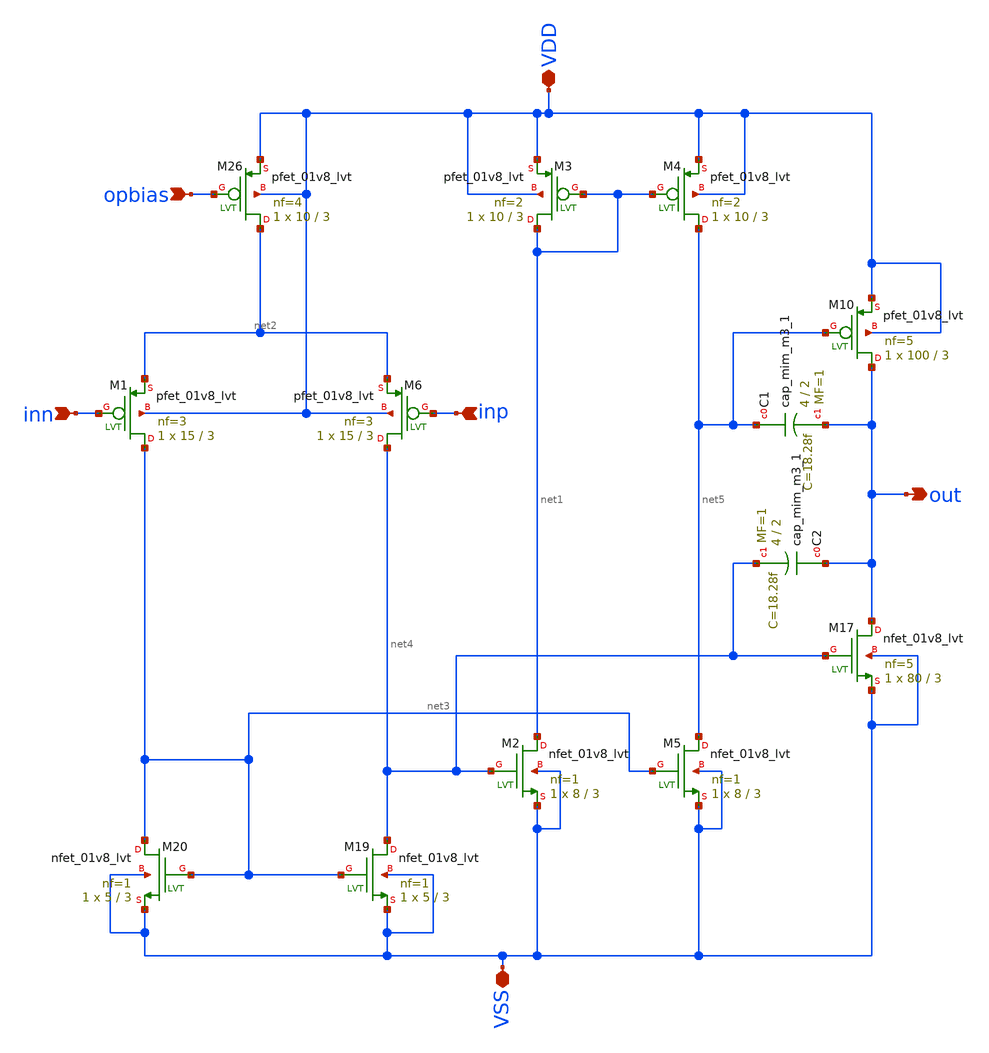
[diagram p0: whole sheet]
** sch_path: xschem/opamp/opamp.sch
**.subckt opamp inp inn opbias out VDD VSS
*.ipin inp
*.ipin inn
*.ipin opbias
*.opin out
*.iopin VDD
*.iopin VSS
XC1 net5 out sky130_fd_pr__cap_mim_m3_1 W=4 L=2 MF=1 m=1
XC2 out net4 sky130_fd_pr__cap_mim_m3_1 W=4 L=2 MF=1 m=1
XM26 net2 opbias VDD VDD sky130_fd_pr__pfet_01v8_lvt L=3 W=10 nf=4 ad='int((4 + 1)/2) * 10 / 4 * 0.29'
+ as='int((4 + 2)/2) * 10 / 4 * 0.29' pd='2*int((4 + 1)/2) * (10 / 4 + 0.29)' ps='2*int((4 + 2)/2) * (10 / 4 + 0.29)'
+ nrd='0.29 / 10 ' nrs='0.29 / 10 ' sa=0 sb=0 sd=0 mult=1 m=1
XM3 net1 net1 VDD VDD sky130_fd_pr__pfet_01v8_lvt L=3 W=10 nf=2 ad='int((2 + 1)/2) * 10 / 2 * 0.29' as='int((2 + 2)/2) * 10 / 2 * 0.29'
+ pd='2*int((2 + 1)/2) * (10 / 2 + 0.29)' ps='2*int((2 + 2)/2) * (10 / 2 + 0.29)' nrd='0.29 / 10 ' nrs='0.29 / 10 '
+ sa=0 sb=0 sd=0 mult=1 m=1
XM4 net5 net1 VDD VDD sky130_fd_pr__pfet_01v8_lvt L=3 W=10 nf=2 ad='int((2 + 1)/2) * 10 / 2 * 0.29' as='int((2 + 2)/2) * 10 / 2 * 0.29'
+ pd='2*int((2 + 1)/2) * (10 / 2 + 0.29)' ps='2*int((2 + 2)/2) * (10 / 2 + 0.29)' nrd='0.29 / 10 ' nrs='0.29 / 10 '
+ sa=0 sb=0 sd=0 mult=1 m=1
XM10 out net5 VDD VDD sky130_fd_pr__pfet_01v8_lvt L=3 W=100 nf=5 ad='int((5 + 1)/2) * 100 / 5 * 0.29'
+ as='int((5 + 2)/2) * 100 / 5 * 0.29' pd='2*int((5 + 1)/2) * (100 / 5 + 0.29)' ps='2*int((5 + 2)/2) * (100 / 5 + 0.29)'
+ nrd='0.29 / 100 ' nrs='0.29 / 100 ' sa=0 sb=0 sd=0 mult=1 m=1
XM17 out net4 VSS VSS sky130_fd_pr__nfet_01v8_lvt L=3 W=80 nf=5 ad='int((5 + 1)/2) * 80 / 5 * 0.29' as='int((5 + 2)/2) * 80 / 5 * 0.29'
+ pd='2*int((5 + 1)/2) * (80 / 5 + 0.29)' ps='2*int((5 + 2)/2) * (80 / 5 + 0.29)' nrd='0.29 / 80 ' nrs='0.29 / 80 '
+ sa=0 sb=0 sd=0 mult=1 m=1
XM19 net4 net3 VSS VSS sky130_fd_pr__nfet_01v8_lvt L=3 W=5 nf=1 ad='int((1 + 1)/2) * 5 / 1 * 0.29' as='int((1 + 2)/2) * 5 / 1 * 0.29'
+ pd='2*int((1 + 1)/2) * (5 / 1 + 0.29)' ps='2*int((1 + 2)/2) * (5 / 1 + 0.29)' nrd='0.29 / 5 ' nrs='0.29 / 5 '
+ sa=0 sb=0 sd=0 mult=1 m=1
XM20 net3 net3 VSS VSS sky130_fd_pr__nfet_01v8_lvt L=3 W=5 nf=1 ad='int((1 + 1)/2) * 5 / 1 * 0.29' as='int((1 + 2)/2) * 5 / 1 * 0.29'
+ pd='2*int((1 + 1)/2) * (5 / 1 + 0.29)' ps='2*int((1 + 2)/2) * (5 / 1 + 0.29)' nrd='0.29 / 5 ' nrs='0.29 / 5 '
+ sa=0 sb=0 sd=0 mult=1 m=1
XM2 net1 net4 VSS VSS sky130_fd_pr__nfet_01v8_lvt L=3 W=8 nf=1 ad='int((1 + 1)/2) * 8 / 1 * 0.29' as='int((1 + 2)/2) * 8 / 1 * 0.29'
+ pd='2*int((1 + 1)/2) * (8 / 1 + 0.29)' ps='2*int((1 + 2)/2) * (8 / 1 + 0.29)' nrd='0.29 / 8 ' nrs='0.29 / 8 '
+ sa=0 sb=0 sd=0 mult=1 m=1
XM5 net5 net3 VSS VSS sky130_fd_pr__nfet_01v8_lvt L=3 W=8 nf=1 ad='int((1 + 1)/2) * 8 / 1 * 0.29' as='int((1 + 2)/2) * 8 / 1 * 0.29'
+ pd='2*int((1 + 1)/2) * (8 / 1 + 0.29)' ps='2*int((1 + 2)/2) * (8 / 1 + 0.29)' nrd='0.29 / 8 ' nrs='0.29 / 8 '
+ sa=0 sb=0 sd=0 mult=1 m=1
XM1 net3 inn net2 VDD sky130_fd_pr__pfet_01v8_lvt L=3 W=15 nf=3 ad='int((3 + 1)/2) * 15 / 3 * 0.29' as='int((3 + 2)/2) * 15 / 3 * 0.29'
+ pd='2*int((3 + 1)/2) * (15 / 3 + 0.29)' ps='2*int((3 + 2)/2) * (15 / 3 + 0.29)' nrd='0.29 / 15 ' nrs='0.29 / 15 '
+ sa=0 sb=0 sd=0 mult=1 m=1
XM6 net4 inp net2 VDD sky130_fd_pr__pfet_01v8_lvt L=3 W=15 nf=3 ad='int((3 + 1)/2) * 15 / 3 * 0.29' as='int((3 + 2)/2) * 15 / 3 * 0.29'
+ pd='2*int((3 + 1)/2) * (15 / 3 + 0.29)' ps='2*int((3 + 2)/2) * (15 / 3 + 0.29)' nrd='0.29 / 15 ' nrs='0.29 / 15 '
+ sa=0 sb=0 sd=0 mult=1 m=1
**.ends
.end
